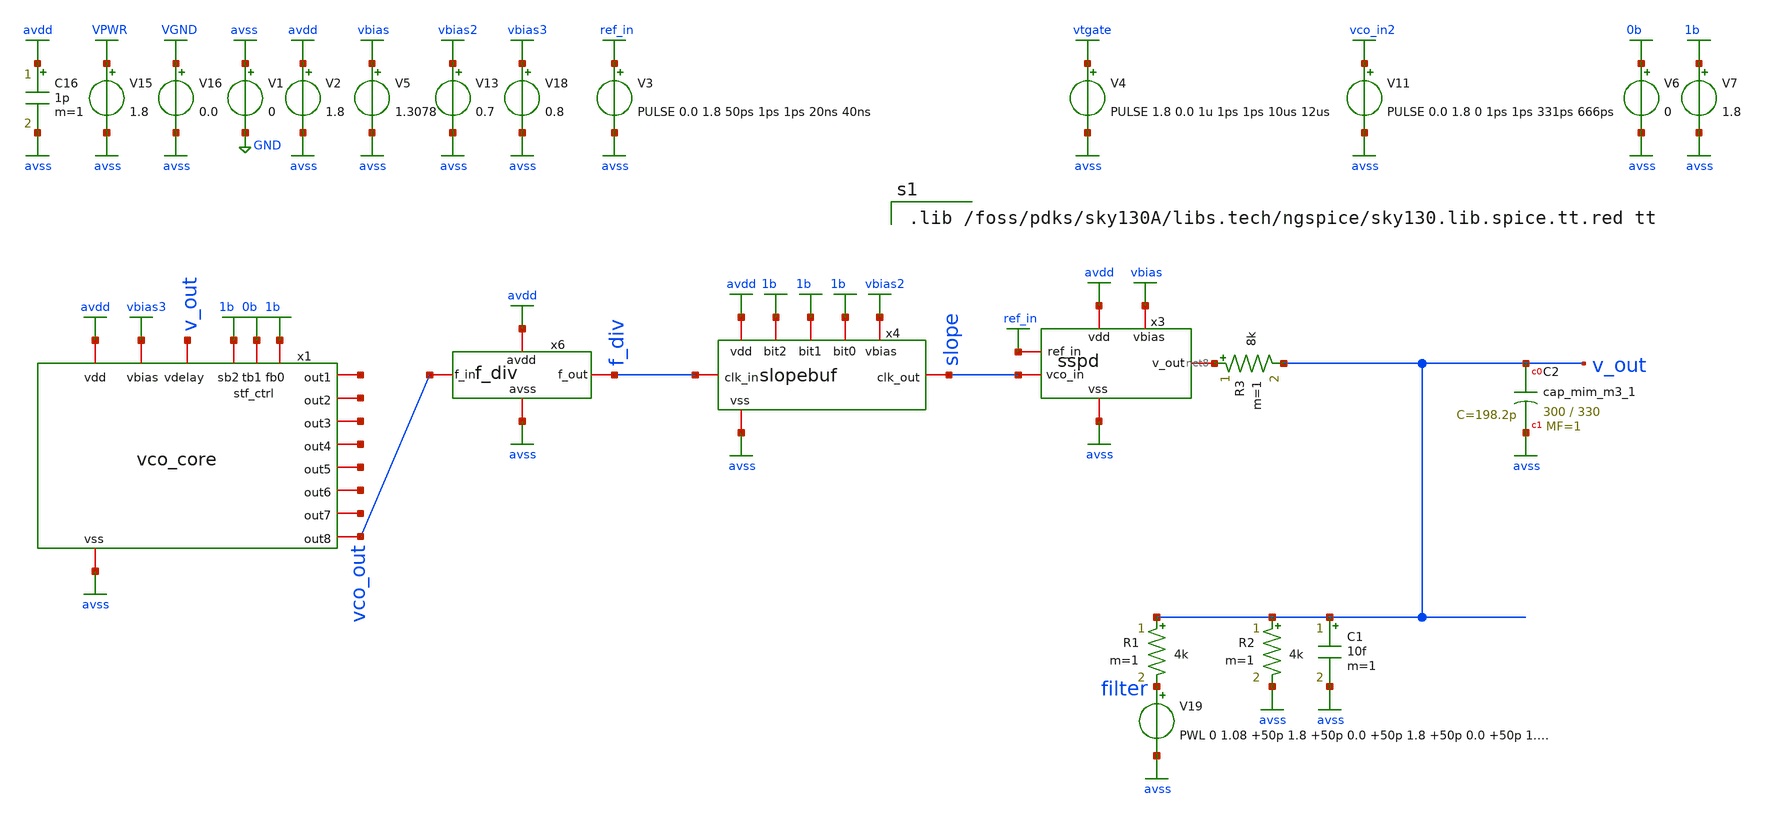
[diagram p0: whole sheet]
** sch_path: xschem/complete_testbench_7.sch
**.subckt complete_testbench_7
V1 avss GND 0
V2 avdd avss 1.8
V3 ref_in avss PULSE 0.0 1.8 50ps 1ps 1ps 20ns 40ns
V5 vbias avss 1.3078
V4 vtgate avss PULSE 1.8 0.0 1u 1ps 1ps 10us 12us
R1 v_out filter 4k m=1
R2 v_out avss 4k m=1
V13 vbias2 avss 0.7
V11 vco_in2 avss PULSE 0.0 1.8 0 1ps 1ps 331ps 666ps
V15 VPWR avss 1.8
V16 VGND avss 0.0
C16 avdd avss 1p m=1
V18 vbias3 avss 0.8
V19 filter avss PWL 0 1.08 +50p 1.8 +50p 0.0 +50p 1.8 +50p 0.0 +50p 1.08 +20n 1.08
x1 avdd net1 avss net2 net3 vbias3 net4 v_out net5 1b 0b net6 net7 1b vco_out vco_core
x3 avdd avss ref_in slope vbias net8 sspd
x4 avdd avss f_div slope 1b 1b 1b vbias2 slopebuf
x6 avdd avss vco_out f_div f_div
V6 0b avss 0
V7 1b avss 1.8
C1 v_out avss 10f m=1
R3 net8 v_out 8k m=1
XC2 v_out avss sky130_fd_pr__cap_mim_m3_1 W=300 L=330 MF=1 m=1
**** begin user architecture code

.lib /foss/pdks/sky130A/libs.tech/ngspice/sky130.lib.spice.tt.red tt



.include /foss/pdks/sky130A/libs.ref/sky130_fd_sc_hd/spice/sky130_fd_sc_hd.spice
.control
*save ref_in vco_out f_div slope v_out @V1[i] @V2[i] @V3[i] @V4[i] @V15[i]
save f_div v_out
tran 0.02n 10000n 0n
run
*plot vco_out
plot f_div
*plot ref_in slope
plot v_out
*plot @V1[i] @V2[i] @V3[i] @V4[i] @V15[i]
*fft ref_in vco_out f_div
*plot db(mag(ref_in)) db(mag(f_div)) db(mag(vco_out)) xlimit 0.1meg 4g ylimit 5 -60
*compose values values 10.738n 10.666n 10.596n
*foreach val $&values
*	echo run = $val
*	alter @v4[pulse] = [ 1.8 0.0 0 5ps 5ps 5.323ns $val ] $ vector
*	save ref_in vco_in clk nclk v_out @V1[i] @V3[i] s1 s2
*	tran 0.001n 280n 40n
*	run
*end
*plot tran1.vco_in tran2.vco_in tran3.vco_in
*plot tran1.s2 tran2.s2 tran3.s2
*plot tran1.v_out tran2.v_out tran3.v_out
*plot tran1.v_out
*plot tran2.v_out
*plot tran3.v_out
*plot tran1.s2
*plot tran2.s2
*plot tran3.s2
*compose values start=0.0 stop=1.8 step=0.1
*foreach val $&values
*	echo run = $val
*	alter v5 $val
*	save ref_in vco_in clk nclk v_out @V1[i] @V3[i] s1 s2
*	tran 0.05n 280n 40n
*	run
*end
.endc
.end


**** end user architecture code
**.ends
.GLOBAL avdd
.GLOBAL avss
.GLOBAL GND
.GLOBAL ref_in
.GLOBAL vbias
.GLOBAL vtgate
.GLOBAL vbias2
.GLOBAL vco_in2
.GLOBAL VPWR
.GLOBAL VGND
.GLOBAL vbias3
.GLOBAL 1b
.GLOBAL 0b
.end
